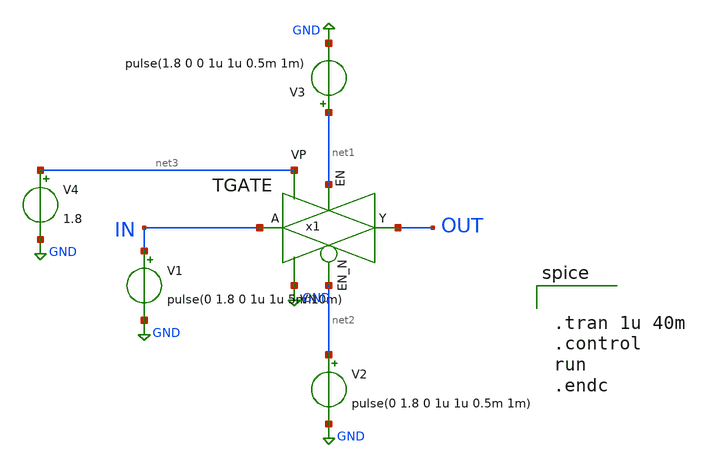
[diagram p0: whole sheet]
** sch_path: ADC/4bit_C2C/MagicAndSpice/EE431_FinalProj/tg_tb.sch
**.subckt tg_tb
V1 IN GND pulse(0 1.8 0 1u 1u 5m 10m)
V2 net2 GND pulse(0 1.8 0 1u 1u 0.5m 1m)
V3 net1 GND pulse(1.8 0 0 1u 1u 0.5m 1m)
x1 IN OUT net1 net2 net3 GND TGATE
V4 net3 GND 1.8
**** begin user architecture code
 .lib $::SKYWATER_MODELS/sky130.lib.spice tt


.tran 1u 40m
.control
run
.endc

**** end user architecture code
**.ends

* expanding   symbol:  TGATE.sym # of pins=6
** sym_path: ADC/16bit_C2C/MagicAndSpice/EE431_FinalProj/TGATE.sym
** sch_path: ADC/16bit_C2C/MagicAndSpice/EE431_FinalProj/TGATE.sch
.subckt TGATE A Y EN EN_N VP VN
*.iopin A
*.iopin Y
*.ipin EN
*.ipin EN_N
*.ipin VP
*.ipin VN
XM5 A EN Y VN sky130_fd_pr__nfet_01v8 L=0.5 W=3 nf=1 ad='int((nf+1)/2) * W/nf * 0.29' as='int((nf+2)/2) * W/nf * 0.29'
+ pd='2*int((nf+1)/2) * (W/nf + 0.29)' ps='2*int((nf+2)/2) * (W/nf + 0.29)' nrd='0.29 / W' nrs='0.29 / W'
+ sa=0 sb=0 sd=0 mult=1 m=1
XM6 A EN_N Y VP sky130_fd_pr__pfet_01v8 L=0.5 W=3 nf=1 ad='int((nf+1)/2) * W/nf * 0.29' as='int((nf+2)/2) * W/nf * 0.29'
+ pd='2*int((nf+1)/2) * (W/nf + 0.29)' ps='2*int((nf+2)/2) * (W/nf + 0.29)' nrd='0.29 / W' nrs='0.29 / W'
+ sa=0 sb=0 sd=0 mult=1 m=1
**** begin user architecture code
type=subcircuit
**** end user architecture code
.ends

.GLOBAL GND
.end
